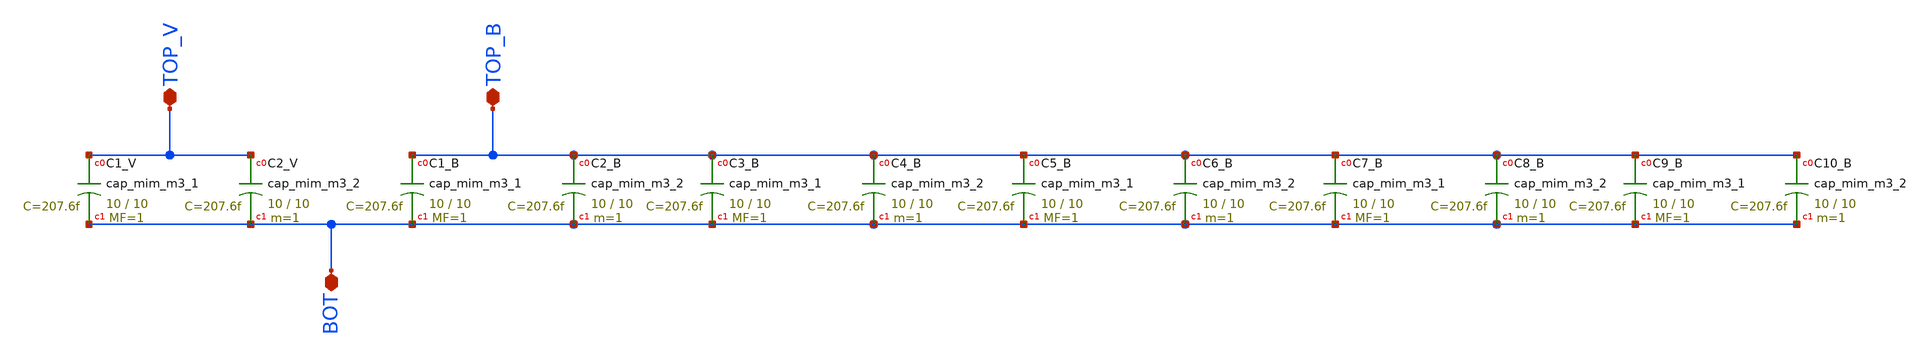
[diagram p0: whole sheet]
** sch_path: samples/cace-tests/SDC/xschem/CAPOSC_v3p1.sch
**.subckt CAPOSC_v3p1 TOP_V TOP_B BOT
*.iopin TOP_V
*.iopin TOP_B
*.iopin BOT
XC1_V TOP_V BOT sky130_fd_pr__cap_mim_m3_1 W=10 L=10 MF=1 m=1
XC2_V TOP_V BOT sky130_fd_pr__cap_mim_m3_2 W=10 L=10 MF=1 m=1
XC1_B TOP_B BOT sky130_fd_pr__cap_mim_m3_1 W=10 L=10 MF=1 m=1
XC2_B TOP_B BOT sky130_fd_pr__cap_mim_m3_2 W=10 L=10 MF=1 m=1
XC5_B TOP_B BOT sky130_fd_pr__cap_mim_m3_1 W=10 L=10 MF=1 m=1
XC6_B TOP_B BOT sky130_fd_pr__cap_mim_m3_2 W=10 L=10 MF=1 m=1
XC3_B TOP_B BOT sky130_fd_pr__cap_mim_m3_1 W=10 L=10 MF=1 m=1
XC4_B TOP_B BOT sky130_fd_pr__cap_mim_m3_2 W=10 L=10 MF=1 m=1
XC7_B TOP_B BOT sky130_fd_pr__cap_mim_m3_1 W=10 L=10 MF=1 m=1
XC8_B TOP_B BOT sky130_fd_pr__cap_mim_m3_2 W=10 L=10 MF=1 m=1
XC9_B TOP_B BOT sky130_fd_pr__cap_mim_m3_1 W=10 L=10 MF=1 m=1
XC10_B TOP_B BOT sky130_fd_pr__cap_mim_m3_2 W=10 L=10 MF=1 m=1
**.ends
.end
